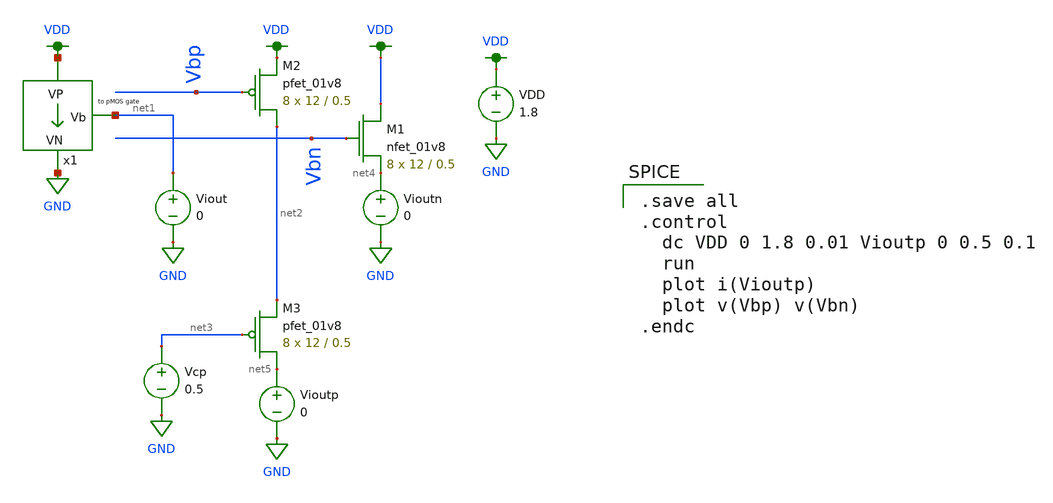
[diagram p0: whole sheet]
** sch_path: schematics/bias/test_current_bias_varying_vout_cascode.sch
**.subckt test_current_bias_varying_vout_cascode
x1 VDD net1 GND current_bias
VDD VDD GND 1.8
Viout net1 GND 0
Vioutn net4 GND 0
XM1 VDD Vbn net4 GND sky130_fd_pr__nfet_01v8 L=0.5 W=12 nf=1 ad='int((nf+1)/2) * W/nf * 0.29' as='int((nf+2)/2) * W/nf * 0.29'
+ pd='2*int((nf+1)/2) * (W/nf + 0.29)' ps='2*int((nf+2)/2) * (W/nf + 0.29)' nrd='0.29 / W' nrs='0.29 / W'
+ sa=0 sb=0 sd=0 mult=8 m=8
XM2 net2 Vbp VDD VDD sky130_fd_pr__pfet_01v8 L=0.5 W=12 nf=1 ad='int((nf+1)/2) * W/nf * 0.29' as='int((nf+2)/2) * W/nf * 0.29'
+ pd='2*int((nf+1)/2) * (W/nf + 0.29)' ps='2*int((nf+2)/2) * (W/nf + 0.29)' nrd='0.29 / W' nrs='0.29 / W'
+ sa=0 sb=0 sd=0 mult=8 m=8
Vioutp net5 GND 0
XM3 net5 net3 net2 VDD sky130_fd_pr__pfet_01v8 L=0.5 W=12 nf=1 ad='int((nf+1)/2) * W/nf * 0.29' as='int((nf+2)/2) * W/nf * 0.29'
+ pd='2*int((nf+1)/2) * (W/nf + 0.29)' ps='2*int((nf+2)/2) * (W/nf + 0.29)' nrd='0.29 / W' nrs='0.29 / W'
+ sa=0 sb=0 sd=0 mult=8 m=8
Vcp net3 GND 0.5
**** begin user architecture code

.option wnflag=1
.param MC_SWITCH=0.0
.lib ~/skywater/skywater-pdk/libraries/sky130_fd_pr_ngspice/latest/models/sky130.lib.spice tt


.save all
.control
  dc VDD 0 1.8 0.01 Vioutp 0 0.5 0.1
  run
  plot i(Vioutp)
  plot v(Vbp) v(Vbn)
.endc

**** end user architecture code
**.ends

* expanding   symbol:
*+  /home/madvlsi/dev/git/7-bit-D-A-converter-MP4-MADVLSI/schematics/bias/current_bias.sym # of pins=3
** sym_path: schematics/bias_2/current_bias.sym
** sch_path: schematics/bias_2/current_bias.sch
.subckt current_bias VP Vb VN
*.iopin VP
*.iopin VN
*.opin Vb
XM4 net1 net1 net4 GND sky130_fd_pr__nfet_01v8 L=0.5 W=12 nf=1 ad='int((nf+1)/2) * W/nf * 0.29' as='int((nf+2)/2) * W/nf * 0.29'
+ pd='2*int((nf+1)/2) * (W/nf + 0.29)' ps='2*int((nf+2)/2) * (W/nf + 0.29)' nrd='0.29 / W' nrs='0.29 / W'
+ sa=0 sb=0 sd=0 mult=8 m=8
XM5 net3 net1 VN GND sky130_fd_pr__nfet_01v8 L=0.5 W=12 nf=1 ad='int((nf+1)/2) * W/nf * 0.29' as='int((nf+2)/2) * W/nf * 0.29'
+ pd='2*int((nf+1)/2) * (W/nf + 0.29)' ps='2*int((nf+2)/2) * (W/nf + 0.29)' nrd='0.29 / W' nrs='0.29 / W'
+ sa=0 sb=0 sd=0 mult=1 m=1
XM6 Vb net2 VN GND sky130_fd_pr__nfet_01v8 L=0.5 W=12 nf=1 ad='int((nf+1)/2) * W/nf * 0.29' as='int((nf+2)/2) * W/nf * 0.29'
+ pd='2*int((nf+1)/2) * (W/nf + 0.29)' ps='2*int((nf+2)/2) * (W/nf + 0.29)' nrd='0.29 / W' nrs='0.29 / W'
+ sa=0 sb=0 sd=0 mult=1 m=1
XM7 net2 net2 VN GND sky130_fd_pr__nfet_01v8 L=0.5 W=12 nf=1 ad='int((nf+1)/2) * W/nf * 0.29' as='int((nf+2)/2) * W/nf * 0.29'
+ pd='2*int((nf+1)/2) * (W/nf + 0.29)' ps='2*int((nf+2)/2) * (W/nf + 0.29)' nrd='0.29 / W' nrs='0.29 / W'
+ sa=0 sb=0 sd=0 mult=1 m=1
R1 net4 VN 100k m=1
XM8 Vb net3 VP VDD sky130_fd_pr__pfet_01v8 L=0.5 W=12 nf=1 ad='int((nf+1)/2) * W/nf * 0.29' as='int((nf+2)/2) * W/nf * 0.29'
+ pd='2*int((nf+1)/2) * (W/nf + 0.29)' ps='2*int((nf+2)/2) * (W/nf + 0.29)' nrd='0.29 / W' nrs='0.29 / W'
+ sa=0 sb=0 sd=0 mult=1 m=1
XM9 net2 Vb VP VDD sky130_fd_pr__pfet_01v8 L=0.5 W=12 nf=1 ad='int((nf+1)/2) * W/nf * 0.29' as='int((nf+2)/2) * W/nf * 0.29'
+ pd='2*int((nf+1)/2) * (W/nf + 0.29)' ps='2*int((nf+2)/2) * (W/nf + 0.29)' nrd='0.29 / W' nrs='0.29 / W'
+ sa=0 sb=0 sd=0 mult=1 m=1
XM10 net3 net3 VP VDD sky130_fd_pr__pfet_01v8 L=0.5 W=12 nf=1 ad='int((nf+1)/2) * W/nf * 0.29' as='int((nf+2)/2) * W/nf * 0.29'
+ pd='2*int((nf+1)/2) * (W/nf + 0.29)' ps='2*int((nf+2)/2) * (W/nf + 0.29)' nrd='0.29 / W' nrs='0.29 / W'
+ sa=0 sb=0 sd=0 mult=1 m=1
XM11 net1 Vb VP VDD sky130_fd_pr__pfet_01v8 L=0.5 W=12 nf=1 ad='int((nf+1)/2) * W/nf * 0.29' as='int((nf+2)/2) * W/nf * 0.29'
+ pd='2*int((nf+1)/2) * (W/nf + 0.29)' ps='2*int((nf+2)/2) * (W/nf + 0.29)' nrd='0.29 / W' nrs='0.29 / W'
+ sa=0 sb=0 sd=0 mult=1 m=1
.ends

.GLOBAL VDD
.GLOBAL GND
.end
